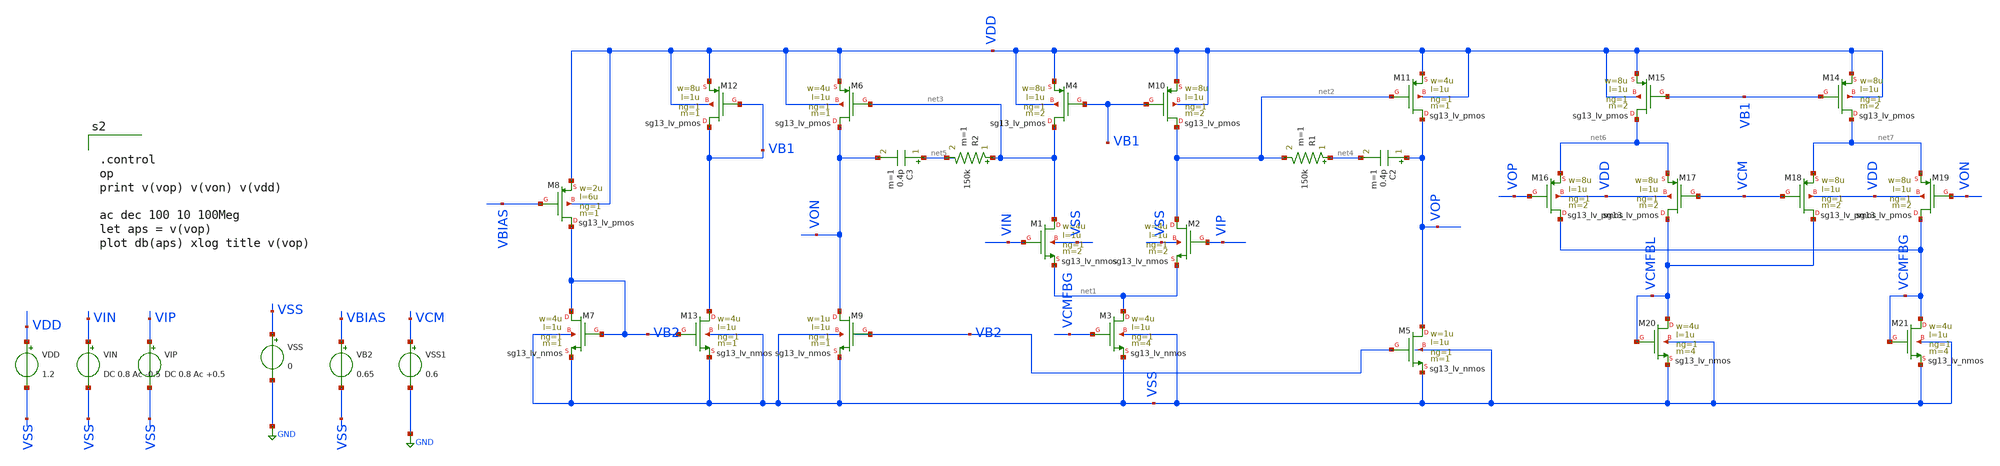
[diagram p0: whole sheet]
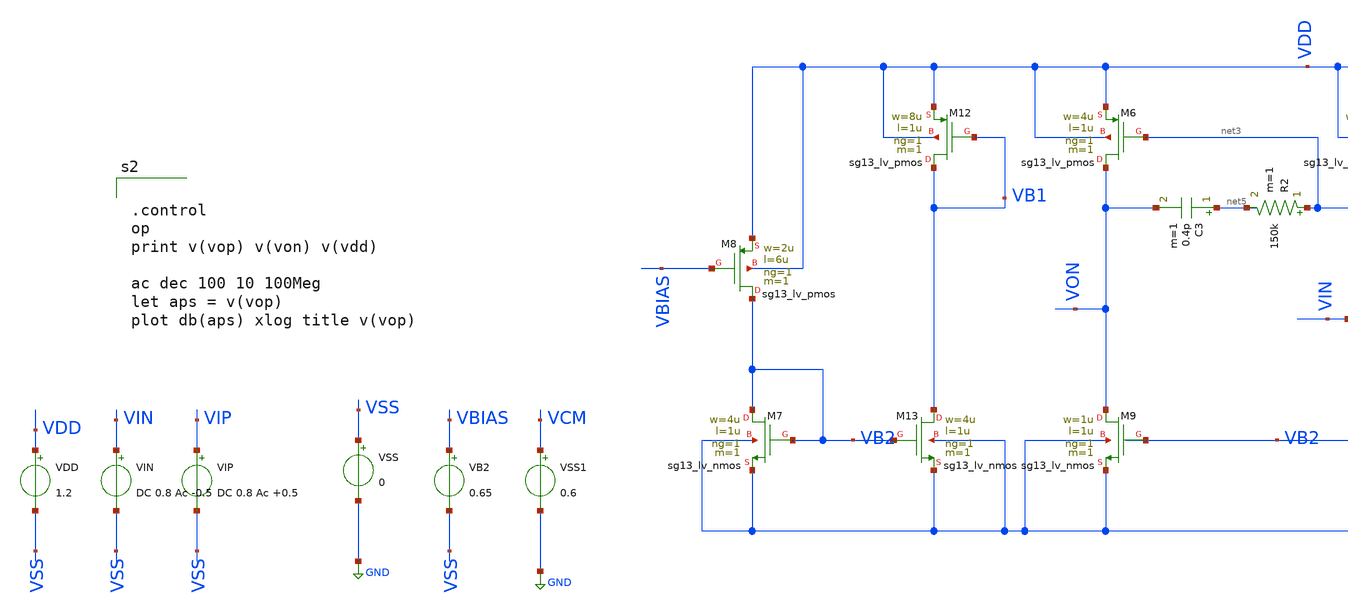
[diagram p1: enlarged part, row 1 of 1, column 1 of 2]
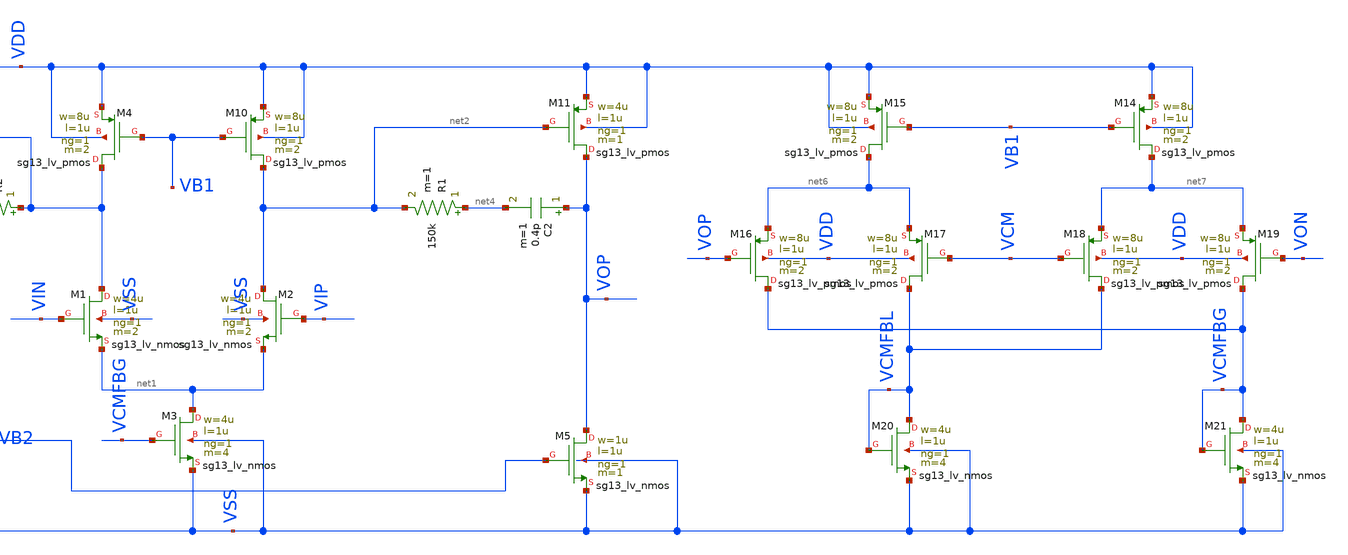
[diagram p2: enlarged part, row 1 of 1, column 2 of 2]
** sch_path: BTDay5-Ex/Ex4_6_Lecture5.sch
**.subckt Ex4_6_Lecture5
XM1 net3 VIN net1 VSS sg13_lv_nmos w=4u l=1u ng=1 m=2 mm_ok=1
XM2 net2 VIP net1 VSS sg13_lv_nmos w=4u l=1u ng=1 m=2 mm_ok=1
XM3 net1 VCMFBG VSS VSS sg13_lv_nmos w=4u l=1u ng=1 m=4 mm_ok=1
VDD VDD VSS 1.2
VIN VIN VSS DC 0.8 Ac -0.5
VIP VIP VSS DC 0.8 Ac +0.5
VSS VSS GND 0
XM4 net3 VB1 VDD VDD sg13_lv_pmos w=8u l=1u ng=1 m=2 mm_ok=1
XM7 VB2 VB2 VSS VSS sg13_lv_nmos w=4u l=1u ng=1 m=1 mm_ok=1
XM8 VB2 VBIAS VDD VDD sg13_lv_pmos w=2u l=6u ng=1 m=1 mm_ok=1
XM10 net2 VB1 VDD VDD sg13_lv_pmos w=8u l=1u ng=1 m=2 mm_ok=1
VB2 VBIAS VSS 0.65
XM5 VOP VB2 VSS VSS sg13_lv_nmos w=1u l=1u ng=1 m=1 mm_ok=1
XM11 VOP net2 VDD VDD sg13_lv_pmos w=4u l=1u ng=1 m=1 mm_ok=1
C2 VOP net4 0.4p m=1
R1 net4 net2 150k m=1
XM9 VON VB2 VSS VSS sg13_lv_nmos w=1u l=1u ng=1 m=1 mm_ok=1
C3 net5 VON 0.4p m=1
R2 net3 net5 150k m=1
XM12 VB1 VB1 VDD VDD sg13_lv_pmos w=8u l=1u ng=1 m=1 mm_ok=1
XM13 VB1 VB2 VSS VSS sg13_lv_nmos w=4u l=1u ng=1 m=1 mm_ok=1
XM6 VON net3 VDD VDD sg13_lv_pmos w=4u l=1u ng=1 m=1 mm_ok=1
XM14 net7 VB1 VDD VDD sg13_lv_pmos w=8u l=1u ng=1 m=2 mm_ok=1
XM15 net6 VB1 VDD VDD sg13_lv_pmos w=8u l=1u ng=1 m=2 mm_ok=1
XM16 VCMFBG VOP net6 VDD sg13_lv_pmos w=8u l=1u ng=1 m=2 mm_ok=1
XM17 VCMFBL VCM net6 VDD sg13_lv_pmos w=8u l=1u ng=1 m=2 mm_ok=1
XM18 VCMFBL VCM net7 VDD sg13_lv_pmos w=8u l=1u ng=1 m=2 mm_ok=1
XM19 VCMFBG VON net7 VDD sg13_lv_pmos w=8u l=1u ng=1 m=2 mm_ok=1
XM20 VCMFBL VCMFBL VSS VSS sg13_lv_nmos w=4u l=1u ng=1 m=4 mm_ok=1
XM21 VCMFBG VCMFBG VSS VSS sg13_lv_nmos w=4u l=1u ng=1 m=4 mm_ok=1
VSS1 VCM GND 0.6
**** begin user architecture code


.lib cornerMOSlv.lib mos_tt




.control
op
print v(vop) v(von) v(vdd)

ac dec 100 10 100Meg
let aps = v(vop)
plot db(aps) xlog title v(vop)

**** end user architecture code
**.ends
.GLOBAL GND
.end
